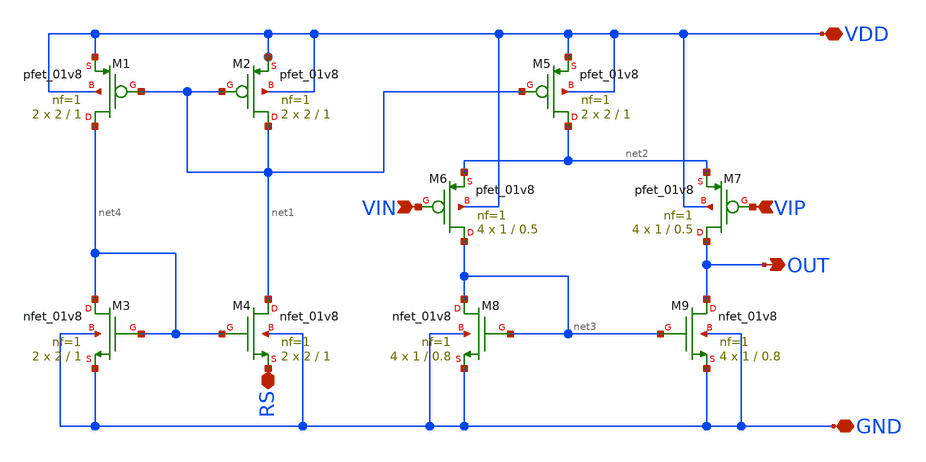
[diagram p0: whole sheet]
** sch_path: OpAmp_Project.sch
**.subckt OpAmp_Project VDD GND RS OUT VIP VIN
*.iopin VDD
*.iopin GND
*.iopin RS
*.opin OUT
*.ipin VIP
*.ipin VIN
XM5 net2 net1 VDD VDD sky130_fd_pr__pfet_01v8 L=1 W=2 nf=1 ad='int((nf+1)/2) * W/nf * 0.29' as='int((nf+2)/2) * W/nf * 0.29'
+ pd='2*int((nf+1)/2) * (W/nf + 0.29)' ps='2*int((nf+2)/2) * (W/nf + 0.29)' nrd='0.29 / W' nrs='0.29 / W'
+ sa=0 sb=0 sd=0 mult=2 m=2
XM2 net1 net1 VDD VDD sky130_fd_pr__pfet_01v8 L=1 W=2 nf=1 ad='int((nf+1)/2) * W/nf * 0.29' as='int((nf+2)/2) * W/nf * 0.29'
+ pd='2*int((nf+1)/2) * (W/nf + 0.29)' ps='2*int((nf+2)/2) * (W/nf + 0.29)' nrd='0.29 / W' nrs='0.29 / W'
+ sa=0 sb=0 sd=0 mult=2 m=2
XM1 net4 net1 VDD VDD sky130_fd_pr__pfet_01v8 L=1 W=2 nf=1 ad='int((nf+1)/2) * W/nf * 0.29' as='int((nf+2)/2) * W/nf * 0.29'
+ pd='2*int((nf+1)/2) * (W/nf + 0.29)' ps='2*int((nf+2)/2) * (W/nf + 0.29)' nrd='0.29 / W' nrs='0.29 / W'
+ sa=0 sb=0 sd=0 mult=2 m=2
XM6 net3 VIN net2 VDD sky130_fd_pr__pfet_01v8 L=0.5 W=1 nf=1 ad='int((nf+1)/2) * W/nf * 0.29' as='int((nf+2)/2) * W/nf * 0.29'
+ pd='2*int((nf+1)/2) * (W/nf + 0.29)' ps='2*int((nf+2)/2) * (W/nf + 0.29)' nrd='0.29 / W' nrs='0.29 / W'
+ sa=0 sb=0 sd=0 mult=4 m=4
XM7 OUT VIP net2 VDD sky130_fd_pr__pfet_01v8 L=0.5 W=1 nf=1 ad='int((nf+1)/2) * W/nf * 0.29' as='int((nf+2)/2) * W/nf * 0.29'
+ pd='2*int((nf+1)/2) * (W/nf + 0.29)' ps='2*int((nf+2)/2) * (W/nf + 0.29)' nrd='0.29 / W' nrs='0.29 / W'
+ sa=0 sb=0 sd=0 mult=4 m=4
XM3 net4 net4 GND GND sky130_fd_pr__nfet_01v8 L=1 W=2 nf=1 ad='int((nf+1)/2) * W/nf * 0.29' as='int((nf+2)/2) * W/nf * 0.29'
+ pd='2*int((nf+1)/2) * (W/nf + 0.29)' ps='2*int((nf+2)/2) * (W/nf + 0.29)' nrd='0.29 / W' nrs='0.29 / W'
+ sa=0 sb=0 sd=0 mult=2 m=2
XM4 net1 net4 RS GND sky130_fd_pr__nfet_01v8 L=1 W=2 nf=1 ad='int((nf+1)/2) * W/nf * 0.29' as='int((nf+2)/2) * W/nf * 0.29'
+ pd='2*int((nf+1)/2) * (W/nf + 0.29)' ps='2*int((nf+2)/2) * (W/nf + 0.29)' nrd='0.29 / W' nrs='0.29 / W'
+ sa=0 sb=0 sd=0 mult=2 m=2
XM8 net3 net3 GND GND sky130_fd_pr__nfet_01v8 L=0.8 W=1 nf=1 ad='int((nf+1)/2) * W/nf * 0.29' as='int((nf+2)/2) * W/nf * 0.29'
+ pd='2*int((nf+1)/2) * (W/nf + 0.29)' ps='2*int((nf+2)/2) * (W/nf + 0.29)' nrd='0.29 / W' nrs='0.29 / W'
+ sa=0 sb=0 sd=0 mult=4 m=4
XM9 OUT net3 GND GND sky130_fd_pr__nfet_01v8 L=0.8 W=1 nf=1 ad='int((nf+1)/2) * W/nf * 0.29' as='int((nf+2)/2) * W/nf * 0.29'
+ pd='2*int((nf+1)/2) * (W/nf + 0.29)' ps='2*int((nf+2)/2) * (W/nf + 0.29)' nrd='0.29 / W' nrs='0.29 / W'
+ sa=0 sb=0 sd=0 mult=4 m=4
**.ends
.end
